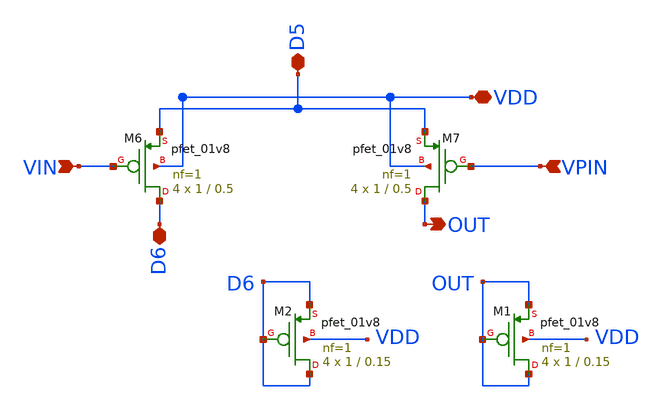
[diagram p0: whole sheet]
** sch_path: differential.sch
**.subckt differential VIN OUT VPIN VDD D6 D5
*.ipin VIN
*.opin OUT
*.ipin VPIN
*.iopin VDD
*.iopin D6
*.iopin D5
XM7 OUT VPIN D5 VDD sky130_fd_pr__pfet_01v8 L=0.5 W=1 nf=1 ad='int((nf+1)/2) * W/nf * 0.29' as='int((nf+2)/2) * W/nf * 0.29'
+ pd='2*int((nf+1)/2) * (W/nf + 0.29)' ps='2*int((nf+2)/2) * (W/nf + 0.29)' nrd='0.29 / W' nrs='0.29 / W'
+ sa=0 sb=0 sd=0 mult=4 m=4
XM6 D6 VIN D5 VDD sky130_fd_pr__pfet_01v8 L=0.5 W=1 nf=1 ad='int((nf+1)/2) * W/nf * 0.29' as='int((nf+2)/2) * W/nf * 0.29'
+ pd='2*int((nf+1)/2) * (W/nf + 0.29)' ps='2*int((nf+2)/2) * (W/nf + 0.29)' nrd='0.29 / W' nrs='0.29 / W'
+ sa=0 sb=0 sd=0 mult=4 m=4
XM1 OUT OUT OUT VDD sky130_fd_pr__pfet_01v8 L=0.15 W=1 nf=1 ad='int((nf+1)/2) * W/nf * 0.29' as='int((nf+2)/2) * W/nf * 0.29'
+ pd='2*int((nf+1)/2) * (W/nf + 0.29)' ps='2*int((nf+2)/2) * (W/nf + 0.29)' nrd='0.29 / W' nrs='0.29 / W'
+ sa=0 sb=0 sd=0 mult=4 m=4
XM2 D6 D6 D6 VDD sky130_fd_pr__pfet_01v8 L=0.15 W=1 nf=1 ad='int((nf+1)/2) * W/nf * 0.29' as='int((nf+2)/2) * W/nf * 0.29'
+ pd='2*int((nf+1)/2) * (W/nf + 0.29)' ps='2*int((nf+2)/2) * (W/nf + 0.29)' nrd='0.29 / W' nrs='0.29 / W'
+ sa=0 sb=0 sd=0 mult=4 m=4
**.ends
.end
